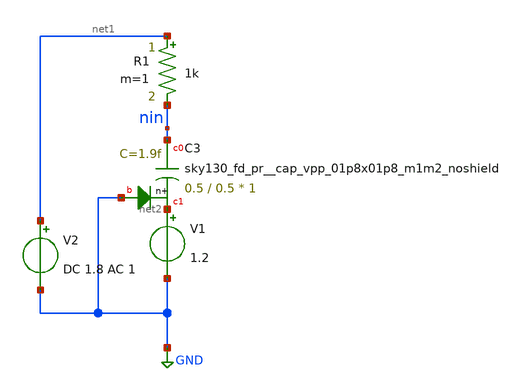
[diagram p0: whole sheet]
** sch_path: xschem/cap_test.sch
**.subckt cap_test
XC3 nin net2 GND sky130_fd_pr__sky130_fd_pr__cap_vpp_01p8x01p8_m1m2_noshield W=0.5 L=0.5 VM=1 m=1
R1 net1 nin 1k m=1
V1 net2 GND 1.2
V2 net1 GND DC 1.8 AC 1
**** begin user architecture code
.lib $::SKYWATER_MODELS/sky130.lib.spice tt
* .include $::PDKPATH/libs.ref/sky130_fd_sc_hvl/spice/sky130_fd_sc_hvl.spice


.subckt  sky130_fd_pr__cap_vpp_01p8x01p8_m1m2_noshield c0 c1 b
.param  mult = 1.0    ctot_a = {7.833e-16*sky130_fd_pr__cap_vpp_01p8x01p8_m1m2_noshield__cor+0.85105/sqrt(mult/0.50527)*MC_MM_SWITCH*AGAUSS(0,0.0183,1)*7.833e-16*sky130_fd_pr__cap_vpp_01p8x01p8_m1m2_noshield__cor}
+  cli2s = {4.548e-17*cli2s_vpp}  rat_m2 = 0.596  rat_m1 = 0.387  rat_m1li = 0.017  cap_m2 = {rat_m2*ctot_a}
+  cap_m1 = {rat_m1*ctot_a}  cap_m1li = {rat_m1li*ctot_a}  nvia_c0 = 8.0  nvia_c1 = 4.0  ncon_c0 = 16.0
rm21 c0 a1 r = {28*rm2}
ccmvpp1p8x1p8 a1 c1  c = {cap_m2}
rvia1 c0 d0 r = {rcvia/nvia_c0}
rvia2 c1 d1 r = {rcvia/nvia_c1}
rm11 d0 b1 r = {22*rm1}
cm1 b1 d1 c = {cap_m1}
rcon d0 e0 r = {rcl1/ncon_c0}
rli1 e0 f0 r = {rl1}
cli2b f0 b c = {cli2s}
cm1li d1 e0 c = {cap_m1li}
.ends sky130_fd_pr__cap_vpp_01p8x01p8_m1m2_noshield
.ac dec 1000 10k 10e9

.control
run
display
plot v(nin)
.endc


**** end user architecture code
**.ends
.GLOBAL GND
.end
